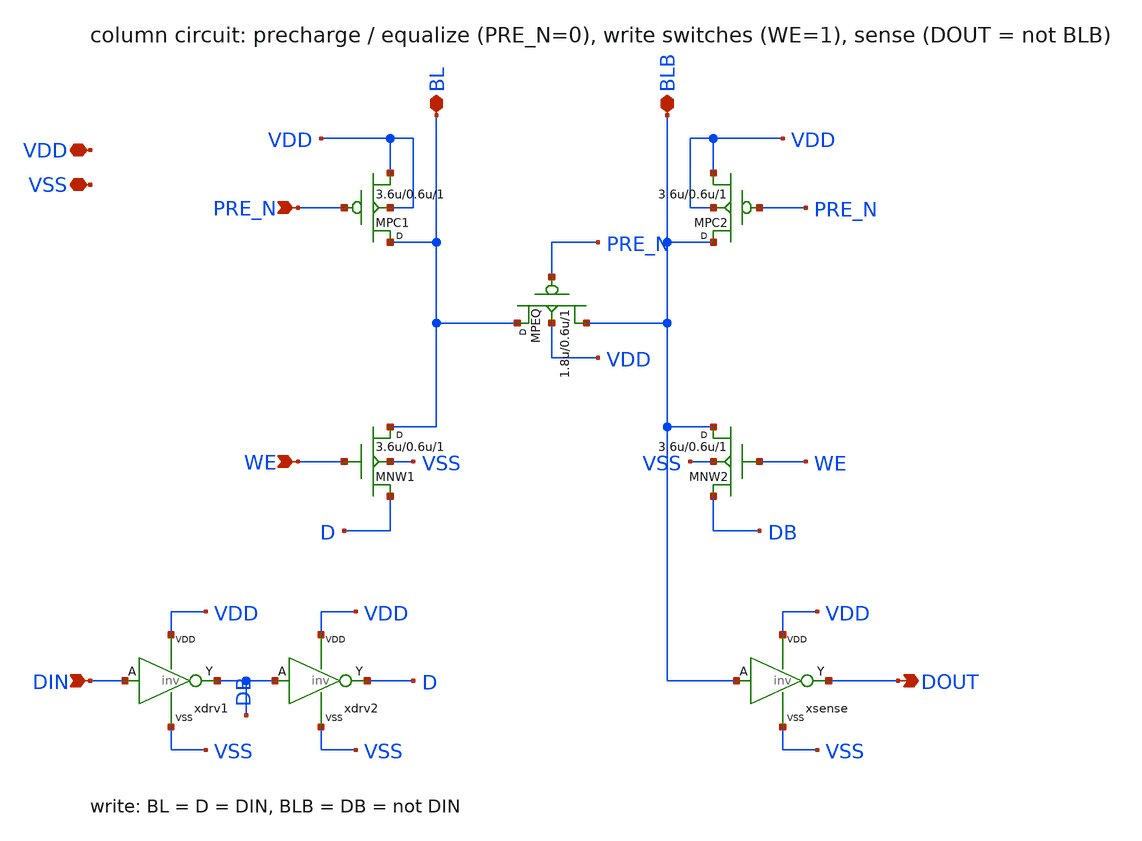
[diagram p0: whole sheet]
** sch_path: sch/column.sch
**.subckt column BL BLB PRE_N WE DIN DOUT VDD VSS
*.iopin BL
*.iopin BLB
*.ipin PRE_N
*.ipin WE
*.ipin DIN
*.opin DOUT
*.iopin VDD
*.iopin VSS
MPC1 BL PRE_N VDD VDD pfet w=3.6u l=0.6u m=1
MPC2 BLB PRE_N VDD VDD pfet w=3.6u l=0.6u m=1
MPEQ BL PRE_N BLB VDD pfet w=1.8u l=0.6u m=1
MNW1 BL WE D VSS nfet w=3.6u l=0.6u m=1
MNW2 BLB WE DB VSS nfet w=3.6u l=0.6u m=1
xdrv1 DIN DB VDD VSS inv
xdrv2 DB D VDD VSS inv
xsense BLB DOUT VDD VSS inv
**.ends

* expanding   symbol:  inv.sym # of pins=4
** sym_path: sch/inv.sym
** sch_path: sch/inv.sch
.subckt inv A Y VDD VSS
*.ipin A
*.opin Y
*.iopin VDD
*.iopin VSS
M1 Y A VDD VDD pfet w=3.6u l=0.6u m=1
M2 Y A VSS VSS nfet w=1.8u l=0.6u m=1
.ends

.end
